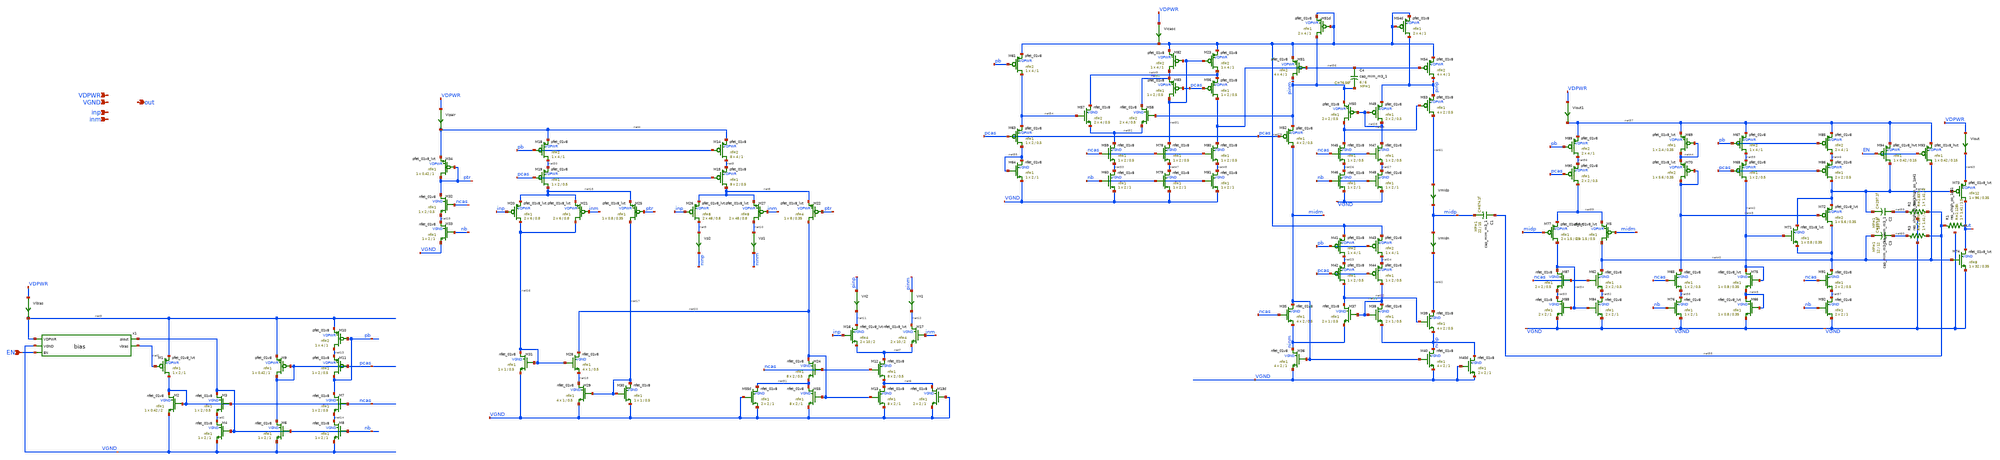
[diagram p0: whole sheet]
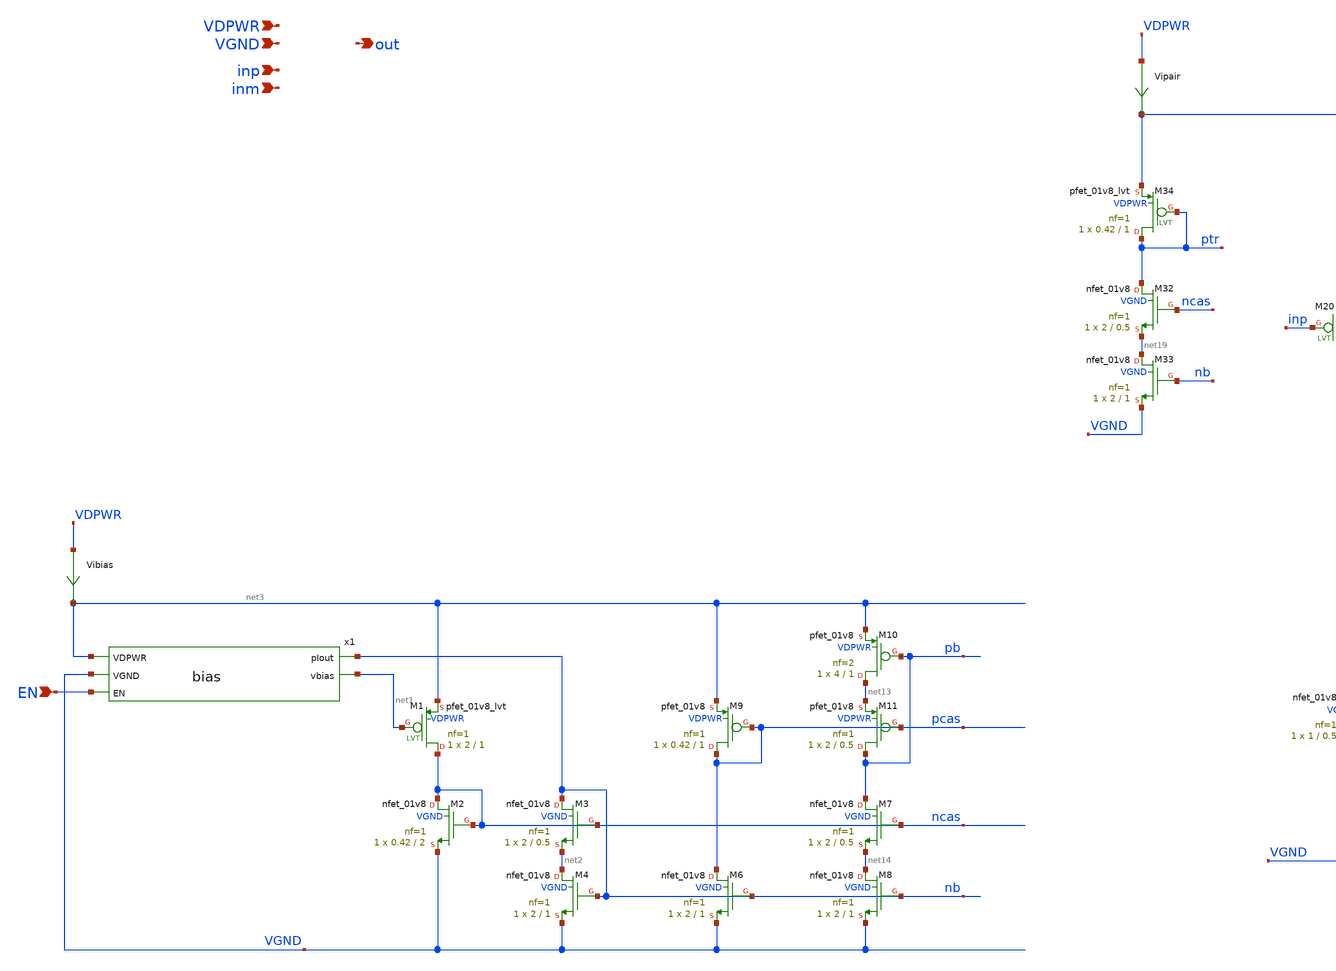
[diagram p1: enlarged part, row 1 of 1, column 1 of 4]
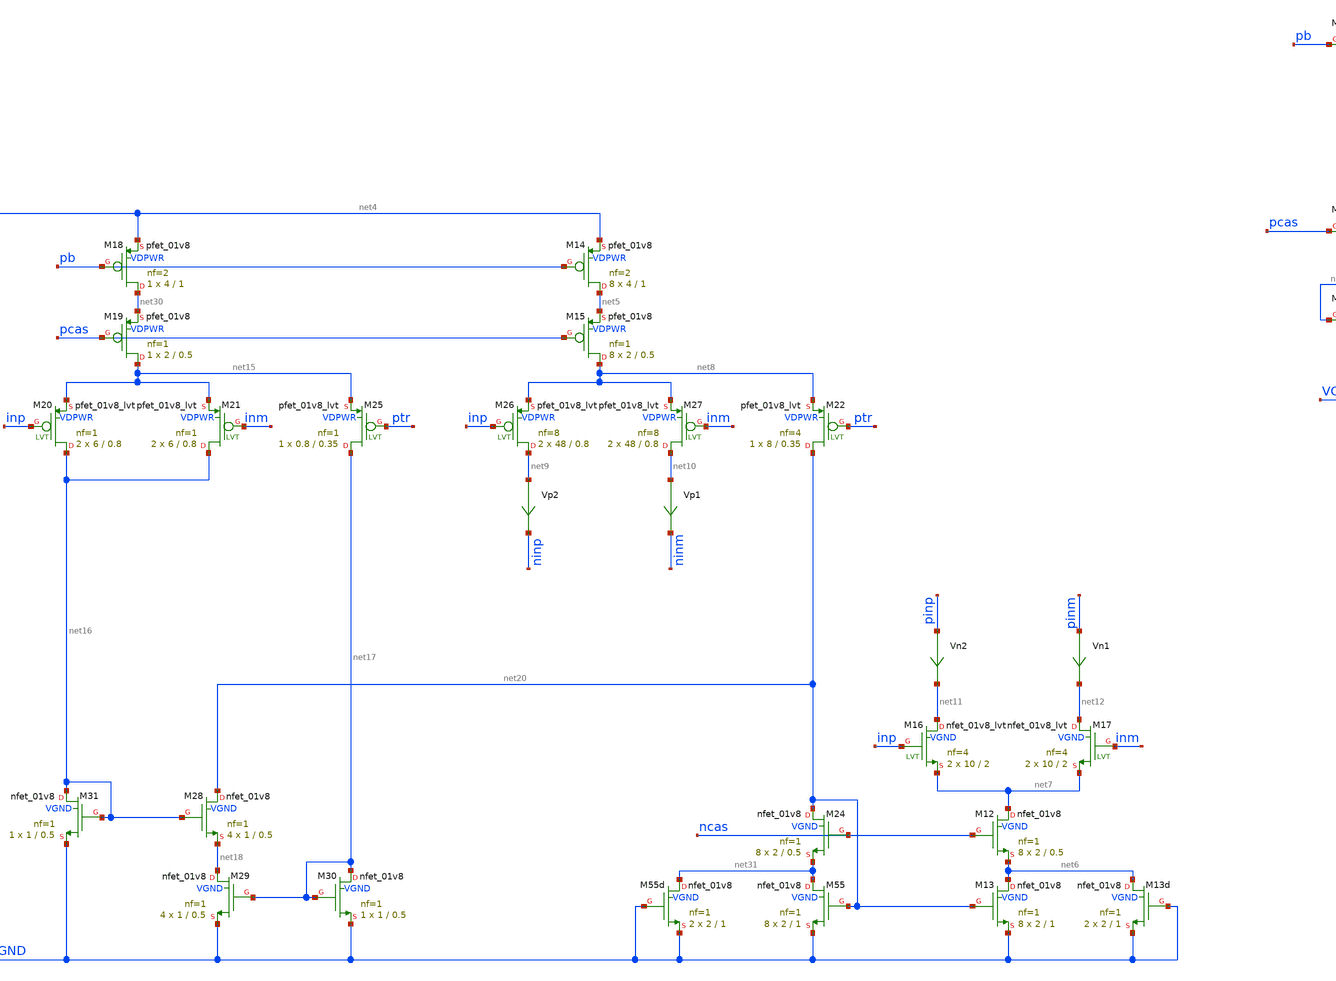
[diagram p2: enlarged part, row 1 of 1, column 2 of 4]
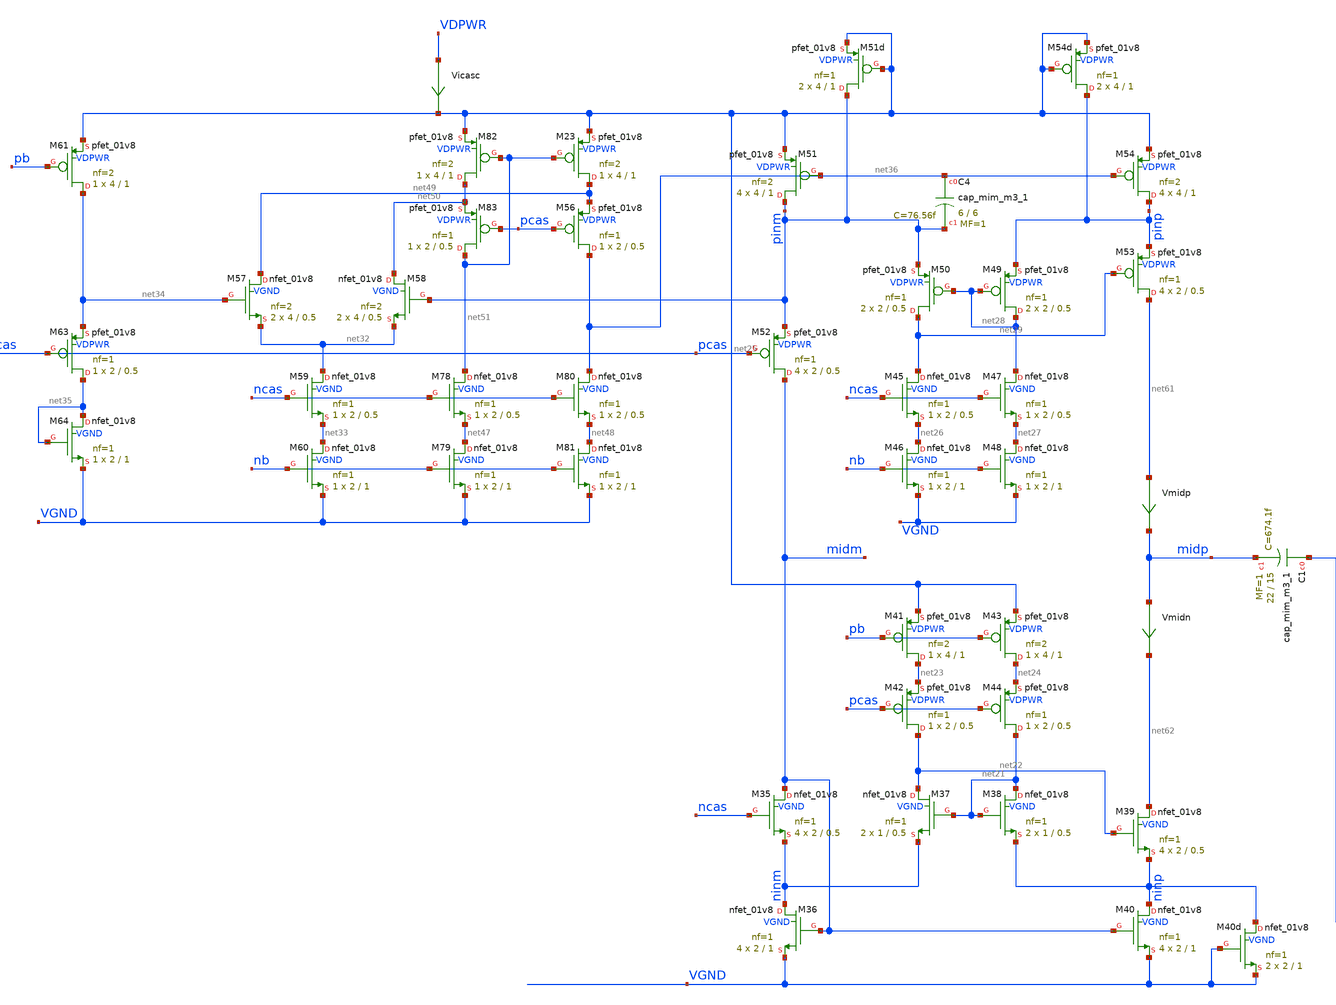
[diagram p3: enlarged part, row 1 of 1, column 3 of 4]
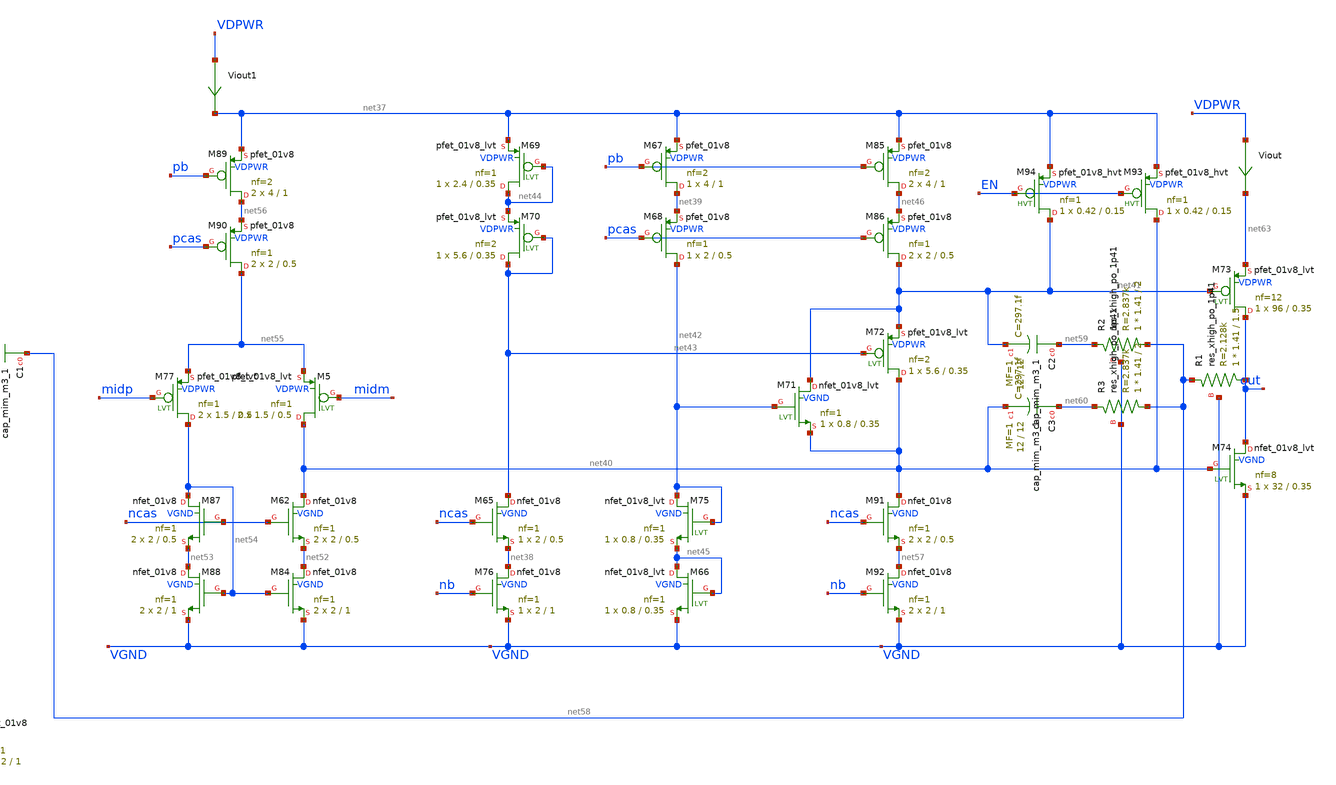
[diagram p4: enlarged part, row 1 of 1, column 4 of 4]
** sch_path: xschem/opamp.sch
**.subckt opamp VDPWR VGND inp inm out EN
*.ipin VDPWR
*.ipin VGND
*.ipin inp
*.ipin inm
*.opin out
*.ipin EN
x1 net3 nb VGND EN net1 bias
XM1 ncas net1 net3 VDPWR sky130_fd_pr__pfet_01v8_lvt L=1 W=2 nf=1 ad='int((1 + 1)/2) * 2 / 1 * 0.29'
+ as='int((1 + 2)/2) * 2 / 1 * 0.29' pd='2*int((1 + 1)/2) * (2 / 1 + 0.29)' ps='2*int((1 + 2)/2) * (2 / 1 + 0.29)'
+ nrd='0.29 / 2 ' nrs='0.29 / 2 ' sa=0 sb=0 sd=0 mult=1 m=1
XM2 ncas ncas VGND VGND sky130_fd_pr__nfet_01v8 L=2 W=0.42 nf=1 ad='int((1 + 1)/2) * 0.42 / 1 * 0.29'
+ as='int((1 + 2)/2) * 0.42 / 1 * 0.29' pd='2*int((1 + 1)/2) * (0.42 / 1 + 0.29)' ps='2*int((1 + 2)/2) * (0.42 / 1 + 0.29)'
+ nrd='0.29 / 0.42 ' nrs='0.29 / 0.42 ' sa=0 sb=0 sd=0 mult=1 m=1
XM3 nb ncas net2 VGND sky130_fd_pr__nfet_01v8 L=0.5 W=2 nf=1 ad='int((1 + 1)/2) * 2 / 1 * 0.29' as='int((1 + 2)/2) * 2 / 1 * 0.29'
+ pd='2*int((1 + 1)/2) * (2 / 1 + 0.29)' ps='2*int((1 + 2)/2) * (2 / 1 + 0.29)' nrd='0.29 / 2 ' nrs='0.29 / 2 '
+ sa=0 sb=0 sd=0 mult=1 m=1
XM4 net2 nb VGND VGND sky130_fd_pr__nfet_01v8 L=1 W=2 nf=1 ad='int((1 + 1)/2) * 2 / 1 * 0.29' as='int((1 + 2)/2) * 2 / 1 * 0.29'
+ pd='2*int((1 + 1)/2) * (2 / 1 + 0.29)' ps='2*int((1 + 2)/2) * (2 / 1 + 0.29)' nrd='0.29 / 2 ' nrs='0.29 / 2 '
+ sa=0 sb=0 sd=0 mult=1 m=1
XM6 pcas nb VGND VGND sky130_fd_pr__nfet_01v8 L=1 W=2 nf=1 ad='int((1 + 1)/2) * 2 / 1 * 0.29' as='int((1 + 2)/2) * 2 / 1 * 0.29'
+ pd='2*int((1 + 1)/2) * (2 / 1 + 0.29)' ps='2*int((1 + 2)/2) * (2 / 1 + 0.29)' nrd='0.29 / 2 ' nrs='0.29 / 2 '
+ sa=0 sb=0 sd=0 mult=1 m=1
XM7 pb ncas net14 VGND sky130_fd_pr__nfet_01v8 L=0.5 W=2 nf=1 ad='int((1 + 1)/2) * 2 / 1 * 0.29' as='int((1 + 2)/2) * 2 / 1 * 0.29'
+ pd='2*int((1 + 1)/2) * (2 / 1 + 0.29)' ps='2*int((1 + 2)/2) * (2 / 1 + 0.29)' nrd='0.29 / 2 ' nrs='0.29 / 2 '
+ sa=0 sb=0 sd=0 mult=1 m=1
XM8 net14 nb VGND VGND sky130_fd_pr__nfet_01v8 L=1 W=2 nf=1 ad='int((1 + 1)/2) * 2 / 1 * 0.29' as='int((1 + 2)/2) * 2 / 1 * 0.29'
+ pd='2*int((1 + 1)/2) * (2 / 1 + 0.29)' ps='2*int((1 + 2)/2) * (2 / 1 + 0.29)' nrd='0.29 / 2 ' nrs='0.29 / 2 '
+ sa=0 sb=0 sd=0 mult=1 m=1
XM9 pcas pcas net3 VDPWR sky130_fd_pr__pfet_01v8 L=1 W=0.42 nf=1 ad='int((1 + 1)/2) * 0.42 / 1 * 0.29'
+ as='int((1 + 2)/2) * 0.42 / 1 * 0.29' pd='2*int((1 + 1)/2) * (0.42 / 1 + 0.29)' ps='2*int((1 + 2)/2) * (0.42 / 1 + 0.29)'
+ nrd='0.29 / 0.42 ' nrs='0.29 / 0.42 ' sa=0 sb=0 sd=0 mult=1 m=1
XM10 net13 pb net3 VDPWR sky130_fd_pr__pfet_01v8 L=1 W=4 nf=2 ad='int((2 + 1)/2) * 4 / 2 * 0.29' as='int((2 + 2)/2) * 4 / 2 * 0.29'
+ pd='2*int((2 + 1)/2) * (4 / 2 + 0.29)' ps='2*int((2 + 2)/2) * (4 / 2 + 0.29)' nrd='0.29 / 4 ' nrs='0.29 / 4 '
+ sa=0 sb=0 sd=0 mult=1 m=1
XM11 pb pcas net13 VDPWR sky130_fd_pr__pfet_01v8 L=0.5 W=2 nf=1 ad='int((1 + 1)/2) * 2 / 1 * 0.29' as='int((1 + 2)/2) * 2 / 1 * 0.29'
+ pd='2*int((1 + 1)/2) * (2 / 1 + 0.29)' ps='2*int((1 + 2)/2) * (2 / 1 + 0.29)' nrd='0.29 / 2 ' nrs='0.29 / 2 '
+ sa=0 sb=0 sd=0 mult=1 m=1
XM12 net7 ncas net6 VGND sky130_fd_pr__nfet_01v8 L=0.5 W=2 nf=1 ad='int((1 + 1)/2) * 2 / 1 * 0.29' as='int((1 + 2)/2) * 2 / 1 * 0.29'
+ pd='2*int((1 + 1)/2) * (2 / 1 + 0.29)' ps='2*int((1 + 2)/2) * (2 / 1 + 0.29)' nrd='0.29 / 2 ' nrs='0.29 / 2 '
+ sa=0 sb=0 sd=0 mult=8 m=8
XM13 net6 net20 VGND VGND sky130_fd_pr__nfet_01v8 L=1 W=2 nf=1 ad='int((1 + 1)/2) * 2 / 1 * 0.29' as='int((1 + 2)/2) * 2 / 1 * 0.29'
+ pd='2*int((1 + 1)/2) * (2 / 1 + 0.29)' ps='2*int((1 + 2)/2) * (2 / 1 + 0.29)' nrd='0.29 / 2 ' nrs='0.29 / 2 '
+ sa=0 sb=0 sd=0 mult=8 m=8
XM14 net5 pb net4 VDPWR sky130_fd_pr__pfet_01v8 L=1 W=4 nf=2 ad='int((2 + 1)/2) * 4 / 2 * 0.29' as='int((2 + 2)/2) * 4 / 2 * 0.29'
+ pd='2*int((2 + 1)/2) * (4 / 2 + 0.29)' ps='2*int((2 + 2)/2) * (4 / 2 + 0.29)' nrd='0.29 / 4 ' nrs='0.29 / 4 '
+ sa=0 sb=0 sd=0 mult=8 m=8
XM15 net8 pcas net5 VDPWR sky130_fd_pr__pfet_01v8 L=0.5 W=2 nf=1 ad='int((1 + 1)/2) * 2 / 1 * 0.29' as='int((1 + 2)/2) * 2 / 1 * 0.29'
+ pd='2*int((1 + 1)/2) * (2 / 1 + 0.29)' ps='2*int((1 + 2)/2) * (2 / 1 + 0.29)' nrd='0.29 / 2 ' nrs='0.29 / 2 '
+ sa=0 sb=0 sd=0 mult=8 m=8
XM16 net11 inp net7 VGND sky130_fd_pr__nfet_01v8_lvt L=2 W=10 nf=4 ad='int((4 + 1)/2) * 10 / 4 * 0.29'
+ as='int((4 + 2)/2) * 10 / 4 * 0.29' pd='2*int((4 + 1)/2) * (10 / 4 + 0.29)' ps='2*int((4 + 2)/2) * (10 / 4 + 0.29)'
+ nrd='0.29 / 10 ' nrs='0.29 / 10 ' sa=0 sb=0 sd=0 mult=2 m=2
XM17 net12 inm net7 VGND sky130_fd_pr__nfet_01v8_lvt L=2 W=10 nf=4 ad='int((4 + 1)/2) * 10 / 4 * 0.29'
+ as='int((4 + 2)/2) * 10 / 4 * 0.29' pd='2*int((4 + 1)/2) * (10 / 4 + 0.29)' ps='2*int((4 + 2)/2) * (10 / 4 + 0.29)'
+ nrd='0.29 / 10 ' nrs='0.29 / 10 ' sa=0 sb=0 sd=0 mult=2 m=2
XM26 net9 inp net8 VDPWR sky130_fd_pr__pfet_01v8_lvt L=0.8 W=48 nf=8 ad='int((8 + 1)/2) * 48 / 8 * 0.29'
+ as='int((8 + 2)/2) * 48 / 8 * 0.29' pd='2*int((8 + 1)/2) * (48 / 8 + 0.29)' ps='2*int((8 + 2)/2) * (48 / 8 + 0.29)'
+ nrd='0.29 / 48 ' nrs='0.29 / 48 ' sa=0 sb=0 sd=0 mult=2 m=2
XM27 net10 inm net8 VDPWR sky130_fd_pr__pfet_01v8_lvt L=0.8 W=48 nf=8 ad='int((8 + 1)/2) * 48 / 8 * 0.29'
+ as='int((8 + 2)/2) * 48 / 8 * 0.29' pd='2*int((8 + 1)/2) * (48 / 8 + 0.29)' ps='2*int((8 + 2)/2) * (48 / 8 + 0.29)'
+ nrd='0.29 / 48 ' nrs='0.29 / 48 ' sa=0 sb=0 sd=0 mult=2 m=2
Vp1 net10 ninm 0
.save i(vp1)
Vp2 net9 ninp 0
.save i(vp2)
Vn1 pinm net12 0
.save i(vn1)
Vn2 pinp net11 0
.save i(vn2)
XM18 net30 pb net4 VDPWR sky130_fd_pr__pfet_01v8 L=1 W=4 nf=2 ad='int((2 + 1)/2) * 4 / 2 * 0.29' as='int((2 + 2)/2) * 4 / 2 * 0.29'
+ pd='2*int((2 + 1)/2) * (4 / 2 + 0.29)' ps='2*int((2 + 2)/2) * (4 / 2 + 0.29)' nrd='0.29 / 4 ' nrs='0.29 / 4 '
+ sa=0 sb=0 sd=0 mult=1 m=1
XM19 net15 pcas net30 VDPWR sky130_fd_pr__pfet_01v8 L=0.5 W=2 nf=1 ad='int((1 + 1)/2) * 2 / 1 * 0.29'
+ as='int((1 + 2)/2) * 2 / 1 * 0.29' pd='2*int((1 + 1)/2) * (2 / 1 + 0.29)' ps='2*int((1 + 2)/2) * (2 / 1 + 0.29)'
+ nrd='0.29 / 2 ' nrs='0.29 / 2 ' sa=0 sb=0 sd=0 mult=1 m=1
XM20 net16 inp net15 VDPWR sky130_fd_pr__pfet_01v8_lvt L=0.8 W=6 nf=1 ad='int((1 + 1)/2) * 6 / 1 * 0.29'
+ as='int((1 + 2)/2) * 6 / 1 * 0.29' pd='2*int((1 + 1)/2) * (6 / 1 + 0.29)' ps='2*int((1 + 2)/2) * (6 / 1 + 0.29)'
+ nrd='0.29 / 6 ' nrs='0.29 / 6 ' sa=0 sb=0 sd=0 mult=2 m=2
XM21 net16 inm net15 VDPWR sky130_fd_pr__pfet_01v8_lvt L=0.8 W=6 nf=1 ad='int((1 + 1)/2) * 6 / 1 * 0.29'
+ as='int((1 + 2)/2) * 6 / 1 * 0.29' pd='2*int((1 + 1)/2) * (6 / 1 + 0.29)' ps='2*int((1 + 2)/2) * (6 / 1 + 0.29)'
+ nrd='0.29 / 6 ' nrs='0.29 / 6 ' sa=0 sb=0 sd=0 mult=2 m=2
XM25 net17 ptr net15 VDPWR sky130_fd_pr__pfet_01v8_lvt L=0.35 W=0.8 nf=1 ad='int((1 + 1)/2) * 0.8 / 1 * 0.29'
+ as='int((1 + 2)/2) * 0.8 / 1 * 0.29' pd='2*int((1 + 1)/2) * (0.8 / 1 + 0.29)' ps='2*int((1 + 2)/2) * (0.8 / 1 + 0.29)'
+ nrd='0.29 / 0.8 ' nrs='0.29 / 0.8 ' sa=0 sb=0 sd=0 mult=1 m=1
XM28 net20 net16 net18 VGND sky130_fd_pr__nfet_01v8 L=0.5 W=1 nf=1 ad='int((1 + 1)/2) * 1 / 1 * 0.29'
+ as='int((1 + 2)/2) * 1 / 1 * 0.29' pd='2*int((1 + 1)/2) * (1 / 1 + 0.29)' ps='2*int((1 + 2)/2) * (1 / 1 + 0.29)'
+ nrd='0.29 / 1 ' nrs='0.29 / 1 ' sa=0 sb=0 sd=0 mult=4 m=4
XM29 net18 net17 VGND VGND sky130_fd_pr__nfet_01v8 L=0.5 W=1 nf=1 ad='int((1 + 1)/2) * 1 / 1 * 0.29'
+ as='int((1 + 2)/2) * 1 / 1 * 0.29' pd='2*int((1 + 1)/2) * (1 / 1 + 0.29)' ps='2*int((1 + 2)/2) * (1 / 1 + 0.29)'
+ nrd='0.29 / 1 ' nrs='0.29 / 1 ' sa=0 sb=0 sd=0 mult=4 m=4
XM30 net17 net17 VGND VGND sky130_fd_pr__nfet_01v8 L=0.5 W=1 nf=1 ad='int((1 + 1)/2) * 1 / 1 * 0.29'
+ as='int((1 + 2)/2) * 1 / 1 * 0.29' pd='2*int((1 + 1)/2) * (1 / 1 + 0.29)' ps='2*int((1 + 2)/2) * (1 / 1 + 0.29)'
+ nrd='0.29 / 1 ' nrs='0.29 / 1 ' sa=0 sb=0 sd=0 mult=1 m=1
XM31 net16 net16 VGND VGND sky130_fd_pr__nfet_01v8 L=0.5 W=1 nf=1 ad='int((1 + 1)/2) * 1 / 1 * 0.29'
+ as='int((1 + 2)/2) * 1 / 1 * 0.29' pd='2*int((1 + 1)/2) * (1 / 1 + 0.29)' ps='2*int((1 + 2)/2) * (1 / 1 + 0.29)'
+ nrd='0.29 / 1 ' nrs='0.29 / 1 ' sa=0 sb=0 sd=0 mult=1 m=1
XM32 ptr ncas net19 VGND sky130_fd_pr__nfet_01v8 L=0.5 W=2 nf=1 ad='int((1 + 1)/2) * 2 / 1 * 0.29' as='int((1 + 2)/2) * 2 / 1 * 0.29'
+ pd='2*int((1 + 1)/2) * (2 / 1 + 0.29)' ps='2*int((1 + 2)/2) * (2 / 1 + 0.29)' nrd='0.29 / 2 ' nrs='0.29 / 2 '
+ sa=0 sb=0 sd=0 mult=1 m=1
XM33 net19 nb VGND VGND sky130_fd_pr__nfet_01v8 L=1 W=2 nf=1 ad='int((1 + 1)/2) * 2 / 1 * 0.29' as='int((1 + 2)/2) * 2 / 1 * 0.29'
+ pd='2*int((1 + 1)/2) * (2 / 1 + 0.29)' ps='2*int((1 + 2)/2) * (2 / 1 + 0.29)' nrd='0.29 / 2 ' nrs='0.29 / 2 '
+ sa=0 sb=0 sd=0 mult=1 m=1
XM34 ptr ptr net4 VDPWR sky130_fd_pr__pfet_01v8_lvt L=1 W=0.42 nf=1 ad='int((1 + 1)/2) * 0.42 / 1 * 0.29'
+ as='int((1 + 2)/2) * 0.42 / 1 * 0.29' pd='2*int((1 + 1)/2) * (0.42 / 1 + 0.29)' ps='2*int((1 + 2)/2) * (0.42 / 1 + 0.29)'
+ nrd='0.29 / 0.42 ' nrs='0.29 / 0.42 ' sa=0 sb=0 sd=0 mult=1 m=1
XM35 midm ncas ninm VGND sky130_fd_pr__nfet_01v8 L=0.5 W=2 nf=1 ad='int((1 + 1)/2) * 2 / 1 * 0.29' as='int((1 + 2)/2) * 2 / 1 * 0.29'
+ pd='2*int((1 + 1)/2) * (2 / 1 + 0.29)' ps='2*int((1 + 2)/2) * (2 / 1 + 0.29)' nrd='0.29 / 2 ' nrs='0.29 / 2 '
+ sa=0 sb=0 sd=0 mult=4 m=4
XM36 ninm midm VGND VGND sky130_fd_pr__nfet_01v8 L=1 W=2 nf=1 ad='int((1 + 1)/2) * 2 / 1 * 0.29' as='int((1 + 2)/2) * 2 / 1 * 0.29'
+ pd='2*int((1 + 1)/2) * (2 / 1 + 0.29)' ps='2*int((1 + 2)/2) * (2 / 1 + 0.29)' nrd='0.29 / 2 ' nrs='0.29 / 2 '
+ sa=0 sb=0 sd=0 mult=4 m=4
XM37 net22 net21 ninm VGND sky130_fd_pr__nfet_01v8 L=0.5 W=1 nf=1 ad='int((1 + 1)/2) * 1 / 1 * 0.29'
+ as='int((1 + 2)/2) * 1 / 1 * 0.29' pd='2*int((1 + 1)/2) * (1 / 1 + 0.29)' ps='2*int((1 + 2)/2) * (1 / 1 + 0.29)'
+ nrd='0.29 / 1 ' nrs='0.29 / 1 ' sa=0 sb=0 sd=0 mult=2 m=2
XM39 net62 net22 ninp VGND sky130_fd_pr__nfet_01v8 L=0.5 W=2 nf=1 ad='int((1 + 1)/2) * 2 / 1 * 0.29'
+ as='int((1 + 2)/2) * 2 / 1 * 0.29' pd='2*int((1 + 1)/2) * (2 / 1 + 0.29)' ps='2*int((1 + 2)/2) * (2 / 1 + 0.29)'
+ nrd='0.29 / 2 ' nrs='0.29 / 2 ' sa=0 sb=0 sd=0 mult=4 m=4
XM40 ninp midm VGND VGND sky130_fd_pr__nfet_01v8 L=1 W=2 nf=1 ad='int((1 + 1)/2) * 2 / 1 * 0.29' as='int((1 + 2)/2) * 2 / 1 * 0.29'
+ pd='2*int((1 + 1)/2) * (2 / 1 + 0.29)' ps='2*int((1 + 2)/2) * (2 / 1 + 0.29)' nrd='0.29 / 2 ' nrs='0.29 / 2 '
+ sa=0 sb=0 sd=0 mult=4 m=4
XM41 net23 pb net25 VDPWR sky130_fd_pr__pfet_01v8 L=1 W=4 nf=2 ad='int((2 + 1)/2) * 4 / 2 * 0.29' as='int((2 + 2)/2) * 4 / 2 * 0.29'
+ pd='2*int((2 + 1)/2) * (4 / 2 + 0.29)' ps='2*int((2 + 2)/2) * (4 / 2 + 0.29)' nrd='0.29 / 4 ' nrs='0.29 / 4 '
+ sa=0 sb=0 sd=0 mult=1 m=1
XM42 net22 pcas net23 VDPWR sky130_fd_pr__pfet_01v8 L=0.5 W=2 nf=1 ad='int((1 + 1)/2) * 2 / 1 * 0.29'
+ as='int((1 + 2)/2) * 2 / 1 * 0.29' pd='2*int((1 + 1)/2) * (2 / 1 + 0.29)' ps='2*int((1 + 2)/2) * (2 / 1 + 0.29)'
+ nrd='0.29 / 2 ' nrs='0.29 / 2 ' sa=0 sb=0 sd=0 mult=1 m=1
XM43 net24 pb net25 VDPWR sky130_fd_pr__pfet_01v8 L=1 W=4 nf=2 ad='int((2 + 1)/2) * 4 / 2 * 0.29' as='int((2 + 2)/2) * 4 / 2 * 0.29'
+ pd='2*int((2 + 1)/2) * (4 / 2 + 0.29)' ps='2*int((2 + 2)/2) * (4 / 2 + 0.29)' nrd='0.29 / 4 ' nrs='0.29 / 4 '
+ sa=0 sb=0 sd=0 mult=1 m=1
XM44 net21 pcas net24 VDPWR sky130_fd_pr__pfet_01v8 L=0.5 W=2 nf=1 ad='int((1 + 1)/2) * 2 / 1 * 0.29'
+ as='int((1 + 2)/2) * 2 / 1 * 0.29' pd='2*int((1 + 1)/2) * (2 / 1 + 0.29)' ps='2*int((1 + 2)/2) * (2 / 1 + 0.29)'
+ nrd='0.29 / 2 ' nrs='0.29 / 2 ' sa=0 sb=0 sd=0 mult=1 m=1
XM45 net29 ncas net26 VGND sky130_fd_pr__nfet_01v8 L=0.5 W=2 nf=1 ad='int((1 + 1)/2) * 2 / 1 * 0.29'
+ as='int((1 + 2)/2) * 2 / 1 * 0.29' pd='2*int((1 + 1)/2) * (2 / 1 + 0.29)' ps='2*int((1 + 2)/2) * (2 / 1 + 0.29)'
+ nrd='0.29 / 2 ' nrs='0.29 / 2 ' sa=0 sb=0 sd=0 mult=1 m=1
XM46 net26 nb VGND VGND sky130_fd_pr__nfet_01v8 L=1 W=2 nf=1 ad='int((1 + 1)/2) * 2 / 1 * 0.29' as='int((1 + 2)/2) * 2 / 1 * 0.29'
+ pd='2*int((1 + 1)/2) * (2 / 1 + 0.29)' ps='2*int((1 + 2)/2) * (2 / 1 + 0.29)' nrd='0.29 / 2 ' nrs='0.29 / 2 '
+ sa=0 sb=0 sd=0 mult=1 m=1
XM47 net28 ncas net27 VGND sky130_fd_pr__nfet_01v8 L=0.5 W=2 nf=1 ad='int((1 + 1)/2) * 2 / 1 * 0.29'
+ as='int((1 + 2)/2) * 2 / 1 * 0.29' pd='2*int((1 + 1)/2) * (2 / 1 + 0.29)' ps='2*int((1 + 2)/2) * (2 / 1 + 0.29)'
+ nrd='0.29 / 2 ' nrs='0.29 / 2 ' sa=0 sb=0 sd=0 mult=1 m=1
XM48 net27 nb VGND VGND sky130_fd_pr__nfet_01v8 L=1 W=2 nf=1 ad='int((1 + 1)/2) * 2 / 1 * 0.29' as='int((1 + 2)/2) * 2 / 1 * 0.29'
+ pd='2*int((1 + 1)/2) * (2 / 1 + 0.29)' ps='2*int((1 + 2)/2) * (2 / 1 + 0.29)' nrd='0.29 / 2 ' nrs='0.29 / 2 '
+ sa=0 sb=0 sd=0 mult=1 m=1
XM50 net29 net28 pinm VDPWR sky130_fd_pr__pfet_01v8 L=0.5 W=2 nf=1 ad='int((1 + 1)/2) * 2 / 1 * 0.29'
+ as='int((1 + 2)/2) * 2 / 1 * 0.29' pd='2*int((1 + 1)/2) * (2 / 1 + 0.29)' ps='2*int((1 + 2)/2) * (2 / 1 + 0.29)'
+ nrd='0.29 / 2 ' nrs='0.29 / 2 ' sa=0 sb=0 sd=0 mult=2 m=2
XM51 pinm net36 net25 VDPWR sky130_fd_pr__pfet_01v8 L=1 W=4 nf=2 ad='int((2 + 1)/2) * 4 / 2 * 0.29' as='int((2 + 2)/2) * 4 / 2 * 0.29'
+ pd='2*int((2 + 1)/2) * (4 / 2 + 0.29)' ps='2*int((2 + 2)/2) * (4 / 2 + 0.29)' nrd='0.29 / 4 ' nrs='0.29 / 4 '
+ sa=0 sb=0 sd=0 mult=4 m=4
XM52 midm pcas pinm VDPWR sky130_fd_pr__pfet_01v8 L=0.5 W=2 nf=1 ad='int((1 + 1)/2) * 2 / 1 * 0.29' as='int((1 + 2)/2) * 2 / 1 * 0.29'
+ pd='2*int((1 + 1)/2) * (2 / 1 + 0.29)' ps='2*int((1 + 2)/2) * (2 / 1 + 0.29)' nrd='0.29 / 2 ' nrs='0.29 / 2 '
+ sa=0 sb=0 sd=0 mult=4 m=4
XM53 net61 net29 pinp VDPWR sky130_fd_pr__pfet_01v8 L=0.5 W=2 nf=1 ad='int((1 + 1)/2) * 2 / 1 * 0.29'
+ as='int((1 + 2)/2) * 2 / 1 * 0.29' pd='2*int((1 + 1)/2) * (2 / 1 + 0.29)' ps='2*int((1 + 2)/2) * (2 / 1 + 0.29)'
+ nrd='0.29 / 2 ' nrs='0.29 / 2 ' sa=0 sb=0 sd=0 mult=4 m=4
XM54 pinp net36 net25 VDPWR sky130_fd_pr__pfet_01v8 L=1 W=4 nf=2 ad='int((2 + 1)/2) * 4 / 2 * 0.29' as='int((2 + 2)/2) * 4 / 2 * 0.29'
+ pd='2*int((2 + 1)/2) * (4 / 2 + 0.29)' ps='2*int((2 + 2)/2) * (4 / 2 + 0.29)' nrd='0.29 / 4 ' nrs='0.29 / 4 '
+ sa=0 sb=0 sd=0 mult=4 m=4
Vibias VDPWR net3 0
.save i(vibias)
Vipair VDPWR net4 0
.save i(vipair)
Vicasc VDPWR net25 0
.save i(vicasc)
XM49 net28 net28 pinp VDPWR sky130_fd_pr__pfet_01v8 L=0.5 W=2 nf=1 ad='int((1 + 1)/2) * 2 / 1 * 0.29'
+ as='int((1 + 2)/2) * 2 / 1 * 0.29' pd='2*int((1 + 1)/2) * (2 / 1 + 0.29)' ps='2*int((1 + 2)/2) * (2 / 1 + 0.29)'
+ nrd='0.29 / 2 ' nrs='0.29 / 2 ' sa=0 sb=0 sd=0 mult=2 m=2
XM38 net21 net21 ninp VGND sky130_fd_pr__nfet_01v8 L=0.5 W=1 nf=1 ad='int((1 + 1)/2) * 1 / 1 * 0.29'
+ as='int((1 + 2)/2) * 1 / 1 * 0.29' pd='2*int((1 + 1)/2) * (1 / 1 + 0.29)' ps='2*int((1 + 2)/2) * (1 / 1 + 0.29)'
+ nrd='0.29 / 1 ' nrs='0.29 / 1 ' sa=0 sb=0 sd=0 mult=2 m=2
XM24 net20 ncas net31 VGND sky130_fd_pr__nfet_01v8 L=0.5 W=2 nf=1 ad='int((1 + 1)/2) * 2 / 1 * 0.29'
+ as='int((1 + 2)/2) * 2 / 1 * 0.29' pd='2*int((1 + 1)/2) * (2 / 1 + 0.29)' ps='2*int((1 + 2)/2) * (2 / 1 + 0.29)'
+ nrd='0.29 / 2 ' nrs='0.29 / 2 ' sa=0 sb=0 sd=0 mult=8 m=8
XM55 net31 net20 VGND VGND sky130_fd_pr__nfet_01v8 L=1 W=2 nf=1 ad='int((1 + 1)/2) * 2 / 1 * 0.29' as='int((1 + 2)/2) * 2 / 1 * 0.29'
+ pd='2*int((1 + 1)/2) * (2 / 1 + 0.29)' ps='2*int((1 + 2)/2) * (2 / 1 + 0.29)' nrd='0.29 / 2 ' nrs='0.29 / 2 '
+ sa=0 sb=0 sd=0 mult=8 m=8
XM22 net20 ptr net8 VDPWR sky130_fd_pr__pfet_01v8_lvt L=0.35 W=8 nf=4 ad='int((4 + 1)/2) * 8 / 4 * 0.29'
+ as='int((4 + 2)/2) * 8 / 4 * 0.29' pd='2*int((4 + 1)/2) * (8 / 4 + 0.29)' ps='2*int((4 + 2)/2) * (8 / 4 + 0.29)'
+ nrd='0.29 / 8 ' nrs='0.29 / 8 ' sa=0 sb=0 sd=0 mult=1 m=1
XM57 net49 net34 net32 VGND sky130_fd_pr__nfet_01v8 L=0.5 W=4 nf=2 ad='int((2 + 1)/2) * 4 / 2 * 0.29'
+ as='int((2 + 2)/2) * 4 / 2 * 0.29' pd='2*int((2 + 1)/2) * (4 / 2 + 0.29)' ps='2*int((2 + 2)/2) * (4 / 2 + 0.29)'
+ nrd='0.29 / 4 ' nrs='0.29 / 4 ' sa=0 sb=0 sd=0 mult=2 m=2
XM58 net50 pinm net32 VGND sky130_fd_pr__nfet_01v8 L=0.5 W=4 nf=2 ad='int((2 + 1)/2) * 4 / 2 * 0.29'
+ as='int((2 + 2)/2) * 4 / 2 * 0.29' pd='2*int((2 + 1)/2) * (4 / 2 + 0.29)' ps='2*int((2 + 2)/2) * (4 / 2 + 0.29)'
+ nrd='0.29 / 4 ' nrs='0.29 / 4 ' sa=0 sb=0 sd=0 mult=2 m=2
XM59 net32 ncas net33 VGND sky130_fd_pr__nfet_01v8 L=0.5 W=2 nf=1 ad='int((1 + 1)/2) * 2 / 1 * 0.29'
+ as='int((1 + 2)/2) * 2 / 1 * 0.29' pd='2*int((1 + 1)/2) * (2 / 1 + 0.29)' ps='2*int((1 + 2)/2) * (2 / 1 + 0.29)'
+ nrd='0.29 / 2 ' nrs='0.29 / 2 ' sa=0 sb=0 sd=0 mult=1 m=1
XM60 net33 nb VGND VGND sky130_fd_pr__nfet_01v8 L=1 W=2 nf=1 ad='int((1 + 1)/2) * 2 / 1 * 0.29' as='int((1 + 2)/2) * 2 / 1 * 0.29'
+ pd='2*int((1 + 1)/2) * (2 / 1 + 0.29)' ps='2*int((1 + 2)/2) * (2 / 1 + 0.29)' nrd='0.29 / 2 ' nrs='0.29 / 2 '
+ sa=0 sb=0 sd=0 mult=1 m=1
XM61 net34 pb net25 VDPWR sky130_fd_pr__pfet_01v8 L=1 W=4 nf=2 ad='int((2 + 1)/2) * 4 / 2 * 0.29' as='int((2 + 2)/2) * 4 / 2 * 0.29'
+ pd='2*int((2 + 1)/2) * (4 / 2 + 0.29)' ps='2*int((2 + 2)/2) * (4 / 2 + 0.29)' nrd='0.29 / 4 ' nrs='0.29 / 4 '
+ sa=0 sb=0 sd=0 mult=1 m=1
XM63 net35 pcas net34 VDPWR sky130_fd_pr__pfet_01v8 L=0.5 W=2 nf=1 ad='int((1 + 1)/2) * 2 / 1 * 0.29'
+ as='int((1 + 2)/2) * 2 / 1 * 0.29' pd='2*int((1 + 1)/2) * (2 / 1 + 0.29)' ps='2*int((1 + 2)/2) * (2 / 1 + 0.29)'
+ nrd='0.29 / 2 ' nrs='0.29 / 2 ' sa=0 sb=0 sd=0 mult=1 m=1
XM64 net35 net35 VGND VGND sky130_fd_pr__nfet_01v8 L=1 W=2 nf=1 ad='int((1 + 1)/2) * 2 / 1 * 0.29' as='int((1 + 2)/2) * 2 / 1 * 0.29'
+ pd='2*int((1 + 1)/2) * (2 / 1 + 0.29)' ps='2*int((1 + 2)/2) * (2 / 1 + 0.29)' nrd='0.29 / 2 ' nrs='0.29 / 2 '
+ sa=0 sb=0 sd=0 mult=1 m=1
XM65 net43 ncas net38 VGND sky130_fd_pr__nfet_01v8 L=0.5 W=2 nf=1 ad='int((1 + 1)/2) * 2 / 1 * 0.29'
+ as='int((1 + 2)/2) * 2 / 1 * 0.29' pd='2*int((1 + 1)/2) * (2 / 1 + 0.29)' ps='2*int((1 + 2)/2) * (2 / 1 + 0.29)'
+ nrd='0.29 / 2 ' nrs='0.29 / 2 ' sa=0 sb=0 sd=0 mult=1 m=1
XM66 net45 net45 VGND VGND sky130_fd_pr__nfet_01v8_lvt L=0.35 W=0.8 nf=1 ad='int((1 + 1)/2) * 0.8 / 1 * 0.29'
+ as='int((1 + 2)/2) * 0.8 / 1 * 0.29' pd='2*int((1 + 1)/2) * (0.8 / 1 + 0.29)' ps='2*int((1 + 2)/2) * (0.8 / 1 + 0.29)'
+ nrd='0.29 / 0.8 ' nrs='0.29 / 0.8 ' sa=0 sb=0 sd=0 mult=1 m=1
XM67 net39 pb net37 VDPWR sky130_fd_pr__pfet_01v8 L=1 W=4 nf=2 ad='int((2 + 1)/2) * 4 / 2 * 0.29' as='int((2 + 2)/2) * 4 / 2 * 0.29'
+ pd='2*int((2 + 1)/2) * (4 / 2 + 0.29)' ps='2*int((2 + 2)/2) * (4 / 2 + 0.29)' nrd='0.29 / 4 ' nrs='0.29 / 4 '
+ sa=0 sb=0 sd=0 mult=1 m=1
XM68 net42 pcas net39 VDPWR sky130_fd_pr__pfet_01v8 L=0.5 W=2 nf=1 ad='int((1 + 1)/2) * 2 / 1 * 0.29'
+ as='int((1 + 2)/2) * 2 / 1 * 0.29' pd='2*int((1 + 1)/2) * (2 / 1 + 0.29)' ps='2*int((1 + 2)/2) * (2 / 1 + 0.29)'
+ nrd='0.29 / 2 ' nrs='0.29 / 2 ' sa=0 sb=0 sd=0 mult=1 m=1
XM69 net44 net44 net37 VDPWR sky130_fd_pr__pfet_01v8_lvt L=0.35 W=2.4 nf=1 ad='int((1 + 1)/2) * 2.4 / 1 * 0.29'
+ as='int((1 + 2)/2) * 2.4 / 1 * 0.29' pd='2*int((1 + 1)/2) * (2.4 / 1 + 0.29)' ps='2*int((1 + 2)/2) * (2.4 / 1 + 0.29)'
+ nrd='0.29 / 2.4 ' nrs='0.29 / 2.4 ' sa=0 sb=0 sd=0 mult=1 m=1
XM70 net43 net43 net44 VDPWR sky130_fd_pr__pfet_01v8_lvt L=0.35 W=5.6 nf=2 ad='int((2 + 1)/2) * 5.6 / 2 * 0.29'
+ as='int((2 + 2)/2) * 5.6 / 2 * 0.29' pd='2*int((2 + 1)/2) * (5.6 / 2 + 0.29)' ps='2*int((2 + 2)/2) * (5.6 / 2 + 0.29)'
+ nrd='0.29 / 5.6 ' nrs='0.29 / 5.6 ' sa=0 sb=0 sd=0 mult=1 m=1
XM71 net41 net42 net40 VGND sky130_fd_pr__nfet_01v8_lvt L=0.35 W=0.8 nf=1 ad='int((1 + 1)/2) * 0.8 / 1 * 0.29'
+ as='int((1 + 2)/2) * 0.8 / 1 * 0.29' pd='2*int((1 + 1)/2) * (0.8 / 1 + 0.29)' ps='2*int((1 + 2)/2) * (0.8 / 1 + 0.29)'
+ nrd='0.29 / 0.8 ' nrs='0.29 / 0.8 ' sa=0 sb=0 sd=0 mult=1 m=1
XM72 net40 net43 net41 VDPWR sky130_fd_pr__pfet_01v8_lvt L=0.35 W=5.6 nf=2 ad='int((2 + 1)/2) * 5.6 / 2 * 0.29'
+ as='int((2 + 2)/2) * 5.6 / 2 * 0.29' pd='2*int((2 + 1)/2) * (5.6 / 2 + 0.29)' ps='2*int((2 + 2)/2) * (5.6 / 2 + 0.29)'
+ nrd='0.29 / 5.6 ' nrs='0.29 / 5.6 ' sa=0 sb=0 sd=0 mult=1 m=1
Viout VDPWR net63 0
.save i(viout)
XM73 out net41 net63 VDPWR sky130_fd_pr__pfet_01v8_lvt L=0.35 W=96 nf=12 ad='int((12 + 1)/2) * 96 / 12 * 0.29'
+ as='int((12 + 2)/2) * 96 / 12 * 0.29' pd='2*int((12 + 1)/2) * (96 / 12 + 0.29)' ps='2*int((12 + 2)/2) * (96 / 12 + 0.29)'
+ nrd='0.29 / 96 ' nrs='0.29 / 96 ' sa=0 sb=0 sd=0 mult=1 m=1
XM74 out net40 VGND VGND sky130_fd_pr__nfet_01v8_lvt L=0.35 W=32 nf=8 ad='int((8 + 1)/2) * 32 / 8 * 0.29'
+ as='int((8 + 2)/2) * 32 / 8 * 0.29' pd='2*int((8 + 1)/2) * (32 / 8 + 0.29)' ps='2*int((8 + 2)/2) * (32 / 8 + 0.29)'
+ nrd='0.29 / 32 ' nrs='0.29 / 32 ' sa=0 sb=0 sd=0 mult=1 m=1
XM75 net42 net42 net45 VGND sky130_fd_pr__nfet_01v8_lvt L=0.35 W=0.8 nf=1 ad='int((1 + 1)/2) * 0.8 / 1 * 0.29'
+ as='int((1 + 2)/2) * 0.8 / 1 * 0.29' pd='2*int((1 + 1)/2) * (0.8 / 1 + 0.29)' ps='2*int((1 + 2)/2) * (0.8 / 1 + 0.29)'
+ nrd='0.29 / 0.8 ' nrs='0.29 / 0.8 ' sa=0 sb=0 sd=0 mult=1 m=1
XM76 net38 nb VGND VGND sky130_fd_pr__nfet_01v8 L=1 W=2 nf=1 ad='int((1 + 1)/2) * 2 / 1 * 0.29' as='int((1 + 2)/2) * 2 / 1 * 0.29'
+ pd='2*int((1 + 1)/2) * (2 / 1 + 0.29)' ps='2*int((1 + 2)/2) * (2 / 1 + 0.29)' nrd='0.29 / 2 ' nrs='0.29 / 2 '
+ sa=0 sb=0 sd=0 mult=1 m=1
XM85 net46 pb net37 VDPWR sky130_fd_pr__pfet_01v8 L=1 W=4 nf=2 ad='int((2 + 1)/2) * 4 / 2 * 0.29' as='int((2 + 2)/2) * 4 / 2 * 0.29'
+ pd='2*int((2 + 1)/2) * (4 / 2 + 0.29)' ps='2*int((2 + 2)/2) * (4 / 2 + 0.29)' nrd='0.29 / 4 ' nrs='0.29 / 4 '
+ sa=0 sb=0 sd=0 mult=2 m=2
XM86 net41 pcas net46 VDPWR sky130_fd_pr__pfet_01v8 L=0.5 W=2 nf=1 ad='int((1 + 1)/2) * 2 / 1 * 0.29'
+ as='int((1 + 2)/2) * 2 / 1 * 0.29' pd='2*int((1 + 1)/2) * (2 / 1 + 0.29)' ps='2*int((1 + 2)/2) * (2 / 1 + 0.29)'
+ nrd='0.29 / 2 ' nrs='0.29 / 2 ' sa=0 sb=0 sd=0 mult=2 m=2
XM77 net54 midp net55 VDPWR sky130_fd_pr__pfet_01v8_lvt L=0.5 W=1.5 nf=1 ad='int((1 + 1)/2) * 1.5 / 1 * 0.29'
+ as='int((1 + 2)/2) * 1.5 / 1 * 0.29' pd='2*int((1 + 1)/2) * (1.5 / 1 + 0.29)' ps='2*int((1 + 2)/2) * (1.5 / 1 + 0.29)'
+ nrd='0.29 / 1.5 ' nrs='0.29 / 1.5 ' sa=0 sb=0 sd=0 mult=2 m=2
Viout1 VDPWR net37 0
.save i(viout1)
XM78 net51 ncas net47 VGND sky130_fd_pr__nfet_01v8 L=0.5 W=2 nf=1 ad='int((1 + 1)/2) * 2 / 1 * 0.29'
+ as='int((1 + 2)/2) * 2 / 1 * 0.29' pd='2*int((1 + 1)/2) * (2 / 1 + 0.29)' ps='2*int((1 + 2)/2) * (2 / 1 + 0.29)'
+ nrd='0.29 / 2 ' nrs='0.29 / 2 ' sa=0 sb=0 sd=0 mult=1 m=1
XM79 net47 nb VGND VGND sky130_fd_pr__nfet_01v8 L=1 W=2 nf=1 ad='int((1 + 1)/2) * 2 / 1 * 0.29' as='int((1 + 2)/2) * 2 / 1 * 0.29'
+ pd='2*int((1 + 1)/2) * (2 / 1 + 0.29)' ps='2*int((1 + 2)/2) * (2 / 1 + 0.29)' nrd='0.29 / 2 ' nrs='0.29 / 2 '
+ sa=0 sb=0 sd=0 mult=1 m=1
XM80 net36 ncas net48 VGND sky130_fd_pr__nfet_01v8 L=0.5 W=2 nf=1 ad='int((1 + 1)/2) * 2 / 1 * 0.29'
+ as='int((1 + 2)/2) * 2 / 1 * 0.29' pd='2*int((1 + 1)/2) * (2 / 1 + 0.29)' ps='2*int((1 + 2)/2) * (2 / 1 + 0.29)'
+ nrd='0.29 / 2 ' nrs='0.29 / 2 ' sa=0 sb=0 sd=0 mult=1 m=1
XM81 net48 nb VGND VGND sky130_fd_pr__nfet_01v8 L=1 W=2 nf=1 ad='int((1 + 1)/2) * 2 / 1 * 0.29' as='int((1 + 2)/2) * 2 / 1 * 0.29'
+ pd='2*int((1 + 1)/2) * (2 / 1 + 0.29)' ps='2*int((1 + 2)/2) * (2 / 1 + 0.29)' nrd='0.29 / 2 ' nrs='0.29 / 2 '
+ sa=0 sb=0 sd=0 mult=1 m=1
XM23 net49 net51 net25 VDPWR sky130_fd_pr__pfet_01v8 L=1 W=4 nf=2 ad='int((2 + 1)/2) * 4 / 2 * 0.29'
+ as='int((2 + 2)/2) * 4 / 2 * 0.29' pd='2*int((2 + 1)/2) * (4 / 2 + 0.29)' ps='2*int((2 + 2)/2) * (4 / 2 + 0.29)'
+ nrd='0.29 / 4 ' nrs='0.29 / 4 ' sa=0 sb=0 sd=0 mult=1 m=1
XM56 net36 pcas net49 VDPWR sky130_fd_pr__pfet_01v8 L=0.5 W=2 nf=1 ad='int((1 + 1)/2) * 2 / 1 * 0.29'
+ as='int((1 + 2)/2) * 2 / 1 * 0.29' pd='2*int((1 + 1)/2) * (2 / 1 + 0.29)' ps='2*int((1 + 2)/2) * (2 / 1 + 0.29)'
+ nrd='0.29 / 2 ' nrs='0.29 / 2 ' sa=0 sb=0 sd=0 mult=1 m=1
XM82 net50 net51 net25 VDPWR sky130_fd_pr__pfet_01v8 L=1 W=4 nf=2 ad='int((2 + 1)/2) * 4 / 2 * 0.29'
+ as='int((2 + 2)/2) * 4 / 2 * 0.29' pd='2*int((2 + 1)/2) * (4 / 2 + 0.29)' ps='2*int((2 + 2)/2) * (4 / 2 + 0.29)'
+ nrd='0.29 / 4 ' nrs='0.29 / 4 ' sa=0 sb=0 sd=0 mult=1 m=1
XM83 net51 pcas net50 VDPWR sky130_fd_pr__pfet_01v8 L=0.5 W=2 nf=1 ad='int((1 + 1)/2) * 2 / 1 * 0.29'
+ as='int((1 + 2)/2) * 2 / 1 * 0.29' pd='2*int((1 + 1)/2) * (2 / 1 + 0.29)' ps='2*int((1 + 2)/2) * (2 / 1 + 0.29)'
+ nrd='0.29 / 2 ' nrs='0.29 / 2 ' sa=0 sb=0 sd=0 mult=1 m=1
XC4 net36 pinm sky130_fd_pr__cap_mim_m3_1 W=6 L=6 MF=1 m=1
XM5 net40 midm net55 VDPWR sky130_fd_pr__pfet_01v8_lvt L=0.5 W=1.5 nf=1 ad='int((1 + 1)/2) * 1.5 / 1 * 0.29'
+ as='int((1 + 2)/2) * 1.5 / 1 * 0.29' pd='2*int((1 + 1)/2) * (1.5 / 1 + 0.29)' ps='2*int((1 + 2)/2) * (1.5 / 1 + 0.29)'
+ nrd='0.29 / 1.5 ' nrs='0.29 / 1.5 ' sa=0 sb=0 sd=0 mult=2 m=2
XM62 net40 ncas net52 VGND sky130_fd_pr__nfet_01v8 L=0.5 W=2 nf=1 ad='int((1 + 1)/2) * 2 / 1 * 0.29'
+ as='int((1 + 2)/2) * 2 / 1 * 0.29' pd='2*int((1 + 1)/2) * (2 / 1 + 0.29)' ps='2*int((1 + 2)/2) * (2 / 1 + 0.29)'
+ nrd='0.29 / 2 ' nrs='0.29 / 2 ' sa=0 sb=0 sd=0 mult=2 m=2
XM84 net52 net54 VGND VGND sky130_fd_pr__nfet_01v8 L=1 W=2 nf=1 ad='int((1 + 1)/2) * 2 / 1 * 0.29' as='int((1 + 2)/2) * 2 / 1 * 0.29'
+ pd='2*int((1 + 1)/2) * (2 / 1 + 0.29)' ps='2*int((1 + 2)/2) * (2 / 1 + 0.29)' nrd='0.29 / 2 ' nrs='0.29 / 2 '
+ sa=0 sb=0 sd=0 mult=2 m=2
XM87 net54 ncas net53 VGND sky130_fd_pr__nfet_01v8 L=0.5 W=2 nf=1 ad='int((1 + 1)/2) * 2 / 1 * 0.29'
+ as='int((1 + 2)/2) * 2 / 1 * 0.29' pd='2*int((1 + 1)/2) * (2 / 1 + 0.29)' ps='2*int((1 + 2)/2) * (2 / 1 + 0.29)'
+ nrd='0.29 / 2 ' nrs='0.29 / 2 ' sa=0 sb=0 sd=0 mult=2 m=2
XM88 net53 net54 VGND VGND sky130_fd_pr__nfet_01v8 L=1 W=2 nf=1 ad='int((1 + 1)/2) * 2 / 1 * 0.29' as='int((1 + 2)/2) * 2 / 1 * 0.29'
+ pd='2*int((1 + 1)/2) * (2 / 1 + 0.29)' ps='2*int((1 + 2)/2) * (2 / 1 + 0.29)' nrd='0.29 / 2 ' nrs='0.29 / 2 '
+ sa=0 sb=0 sd=0 mult=2 m=2
XM89 net56 pb net37 VDPWR sky130_fd_pr__pfet_01v8 L=1 W=4 nf=2 ad='int((2 + 1)/2) * 4 / 2 * 0.29' as='int((2 + 2)/2) * 4 / 2 * 0.29'
+ pd='2*int((2 + 1)/2) * (4 / 2 + 0.29)' ps='2*int((2 + 2)/2) * (4 / 2 + 0.29)' nrd='0.29 / 4 ' nrs='0.29 / 4 '
+ sa=0 sb=0 sd=0 mult=2 m=2
XM90 net55 pcas net56 VDPWR sky130_fd_pr__pfet_01v8 L=0.5 W=2 nf=1 ad='int((1 + 1)/2) * 2 / 1 * 0.29'
+ as='int((1 + 2)/2) * 2 / 1 * 0.29' pd='2*int((1 + 1)/2) * (2 / 1 + 0.29)' ps='2*int((1 + 2)/2) * (2 / 1 + 0.29)'
+ nrd='0.29 / 2 ' nrs='0.29 / 2 ' sa=0 sb=0 sd=0 mult=2 m=2
XM91 net40 ncas net57 VGND sky130_fd_pr__nfet_01v8 L=0.5 W=2 nf=1 ad='int((1 + 1)/2) * 2 / 1 * 0.29'
+ as='int((1 + 2)/2) * 2 / 1 * 0.29' pd='2*int((1 + 1)/2) * (2 / 1 + 0.29)' ps='2*int((1 + 2)/2) * (2 / 1 + 0.29)'
+ nrd='0.29 / 2 ' nrs='0.29 / 2 ' sa=0 sb=0 sd=0 mult=2 m=2
XM92 net57 nb VGND VGND sky130_fd_pr__nfet_01v8 L=1 W=2 nf=1 ad='int((1 + 1)/2) * 2 / 1 * 0.29' as='int((1 + 2)/2) * 2 / 1 * 0.29'
+ pd='2*int((1 + 1)/2) * (2 / 1 + 0.29)' ps='2*int((1 + 2)/2) * (2 / 1 + 0.29)' nrd='0.29 / 2 ' nrs='0.29 / 2 '
+ sa=0 sb=0 sd=0 mult=2 m=2
XC1 net58 midp sky130_fd_pr__cap_mim_m3_1 W=22 L=15 MF=1 m=1
XC2 net59 net41 sky130_fd_pr__cap_mim_m3_1 W=12 L=12 MF=1 m=1
XC3 net60 net40 sky130_fd_pr__cap_mim_m3_1 W=12 L=12 MF=1 m=1
XR1 out net58 VGND sky130_fd_pr__res_xhigh_po_1p41 L=1.5 mult=1 m=1
XR2 net58 net59 VGND sky130_fd_pr__res_xhigh_po_1p41 L=2 mult=1 m=1
XR3 net58 net60 VGND sky130_fd_pr__res_xhigh_po_1p41 L=2 mult=1 m=1
Vmidn midp net62 0
.save i(vmidn)
Vmidp net61 midp 0
.save i(vmidp)
XM94 net41 EN net37 VDPWR sky130_fd_pr__pfet_01v8_hvt L=0.15 W=0.42 nf=1 ad='int((1 + 1)/2) * 0.42 / 1 * 0.29'
+ as='int((1 + 2)/2) * 0.42 / 1 * 0.29' pd='2*int((1 + 1)/2) * (0.42 / 1 + 0.29)' ps='2*int((1 + 2)/2) * (0.42 / 1 + 0.29)'
+ nrd='0.29 / 0.42 ' nrs='0.29 / 0.42 ' sa=0 sb=0 sd=0 mult=1 m=1
XM93 net40 EN net37 VDPWR sky130_fd_pr__pfet_01v8_hvt L=0.15 W=0.42 nf=1 ad='int((1 + 1)/2) * 0.42 / 1 * 0.29'
+ as='int((1 + 2)/2) * 0.42 / 1 * 0.29' pd='2*int((1 + 1)/2) * (0.42 / 1 + 0.29)' ps='2*int((1 + 2)/2) * (0.42 / 1 + 0.29)'
+ nrd='0.29 / 0.42 ' nrs='0.29 / 0.42 ' sa=0 sb=0 sd=0 mult=1 m=1
XM55d net31 VGND VGND VGND sky130_fd_pr__nfet_01v8 L=1 W=2 nf=1 ad='int((1 + 1)/2) * 2 / 1 * 0.29' as='int((1 + 2)/2) * 2 / 1 * 0.29'
+ pd='2*int((1 + 1)/2) * (2 / 1 + 0.29)' ps='2*int((1 + 2)/2) * (2 / 1 + 0.29)' nrd='0.29 / 2 ' nrs='0.29 / 2 '
+ sa=0 sb=0 sd=0 mult=2 m=2
XM13d net6 VGND VGND VGND sky130_fd_pr__nfet_01v8 L=1 W=2 nf=1 ad='int((1 + 1)/2) * 2 / 1 * 0.29' as='int((1 + 2)/2) * 2 / 1 * 0.29'
+ pd='2*int((1 + 1)/2) * (2 / 1 + 0.29)' ps='2*int((1 + 2)/2) * (2 / 1 + 0.29)' nrd='0.29 / 2 ' nrs='0.29 / 2 '
+ sa=0 sb=0 sd=0 mult=2 m=2
XM51d pinm net25 net25 VDPWR sky130_fd_pr__pfet_01v8 L=1 W=4 nf=1 ad='int((1 + 1)/2) * 4 / 1 * 0.29'
+ as='int((1 + 2)/2) * 4 / 1 * 0.29' pd='2*int((1 + 1)/2) * (4 / 1 + 0.29)' ps='2*int((1 + 2)/2) * (4 / 1 + 0.29)'
+ nrd='0.29 / 4 ' nrs='0.29 / 4 ' sa=0 sb=0 sd=0 mult=2 m=2
XM54d pinp net25 net25 VDPWR sky130_fd_pr__pfet_01v8 L=1 W=4 nf=1 ad='int((1 + 1)/2) * 4 / 1 * 0.29'
+ as='int((1 + 2)/2) * 4 / 1 * 0.29' pd='2*int((1 + 1)/2) * (4 / 1 + 0.29)' ps='2*int((1 + 2)/2) * (4 / 1 + 0.29)'
+ nrd='0.29 / 4 ' nrs='0.29 / 4 ' sa=0 sb=0 sd=0 mult=2 m=2
XM40d ninp VGND VGND VGND sky130_fd_pr__nfet_01v8 L=1 W=2 nf=1 ad='int((1 + 1)/2) * 2 / 1 * 0.29' as='int((1 + 2)/2) * 2 / 1 * 0.29'
+ pd='2*int((1 + 1)/2) * (2 / 1 + 0.29)' ps='2*int((1 + 2)/2) * (2 / 1 + 0.29)' nrd='0.29 / 2 ' nrs='0.29 / 2 '
+ sa=0 sb=0 sd=0 mult=2 m=2
**.ends

* expanding   symbol:  /foss/designs/ttsky26c-analog-park/xschem/bias.sym # of pins=5
** sym_path: xschem/bias.sym
** sch_path: xschem/bias.sch
.subckt bias VDPWR pIout VGND EN vbias
*.ipin EN
*.opin pIout
*.ipin VGND
*.ipin VDPWR
*.opin vbias
XM4 inm vbias VDPWR VDPWR sky130_fd_pr__pfet_01v8_lvt L=2 W=2 nf=1 ad='int((1 + 1)/2) * 2 / 1 * 0.29'
+ as='int((1 + 2)/2) * 2 / 1 * 0.29' pd='2*int((1 + 1)/2) * (2 / 1 + 0.29)' ps='2*int((1 + 2)/2) * (2 / 1 + 0.29)'
+ nrd='0.29 / 2 ' nrs='0.29 / 2 ' sa=0 sb=0 sd=0 mult=2 m=2
XM2 inp vbias VDPWR VDPWR sky130_fd_pr__pfet_01v8_lvt L=2 W=2 nf=1 ad='int((1 + 1)/2) * 2 / 1 * 0.29'
+ as='int((1 + 2)/2) * 2 / 1 * 0.29' pd='2*int((1 + 1)/2) * (2 / 1 + 0.29)' ps='2*int((1 + 2)/2) * (2 / 1 + 0.29)'
+ nrd='0.29 / 2 ' nrs='0.29 / 2 ' sa=0 sb=0 sd=0 mult=2 m=2
XM5 pIout vbias VDPWR VDPWR sky130_fd_pr__pfet_01v8_lvt L=2 W=2 nf=1 ad='int((1 + 1)/2) * 2 / 1 * 0.29'
+ as='int((1 + 2)/2) * 2 / 1 * 0.29' pd='2*int((1 + 1)/2) * (2 / 1 + 0.29)' ps='2*int((1 + 2)/2) * (2 / 1 + 0.29)'
+ nrd='0.29 / 2 ' nrs='0.29 / 2 ' sa=0 sb=0 sd=0 mult=2 m=2
XM8 inm inm VGND VGND sky130_fd_pr__nfet_01v8 L=2 W=4 nf=1 ad='int((1 + 1)/2) * 4 / 1 * 0.29' as='int((1 + 2)/2) * 4 / 1 * 0.29'
+ pd='2*int((1 + 1)/2) * (4 / 1 + 0.29)' ps='2*int((1 + 2)/2) * (4 / 1 + 0.29)' nrd='0.29 / 4 ' nrs='0.29 / 4 '
+ sa=0 sb=0 sd=0 mult=1 m=1
XM9 inp inp net1 VGND sky130_fd_pr__nfet_01v8 L=2 W=4 nf=1 ad='int((1 + 1)/2) * 4 / 1 * 0.29' as='int((1 + 2)/2) * 4 / 1 * 0.29'
+ pd='2*int((1 + 1)/2) * (4 / 1 + 0.29)' ps='2*int((1 + 2)/2) * (4 / 1 + 0.29)' nrd='0.29 / 4 ' nrs='0.29 / 4 '
+ sa=0 sb=0 sd=0 mult=4 m=4
XM10 net2 inp VGND VGND sky130_fd_pr__nfet_01v8 L=2 W=2 nf=1 ad='int((1 + 1)/2) * 2 / 1 * 0.29' as='int((1 + 2)/2) * 2 / 1 * 0.29'
+ pd='2*int((1 + 1)/2) * (2 / 1 + 0.29)' ps='2*int((1 + 2)/2) * (2 / 1 + 0.29)' nrd='0.29 / 2 ' nrs='0.29 / 2 '
+ sa=0 sb=0 sd=0 mult=2 m=2
XM11 vbias inm VGND VGND sky130_fd_pr__nfet_01v8 L=2 W=2 nf=1 ad='int((1 + 1)/2) * 2 / 1 * 0.29' as='int((1 + 2)/2) * 2 / 1 * 0.29'
+ pd='2*int((1 + 1)/2) * (2 / 1 + 0.29)' ps='2*int((1 + 2)/2) * (2 / 1 + 0.29)' nrd='0.29 / 2 ' nrs='0.29 / 2 '
+ sa=0 sb=0 sd=0 mult=2 m=2
XM15 vbias startup inm VGND sky130_fd_pr__nfet_01v8_lvt L=0.15 W=0.5 nf=1 ad='int((1 + 1)/2) * 0.5 / 1 * 0.29'
+ as='int((1 + 2)/2) * 0.5 / 1 * 0.29' pd='2*int((1 + 1)/2) * (0.5 / 1 + 0.29)' ps='2*int((1 + 2)/2) * (0.5 / 1 + 0.29)'
+ nrd='0.29 / 0.5 ' nrs='0.29 / 0.5 ' sa=0 sb=0 sd=0 mult=1 m=1
XM3 startup inm VGND VGND sky130_fd_pr__nfet_01v8 L=0.5 W=0.5 nf=1 ad='int((1 + 1)/2) * 0.5 / 1 * 0.29'
+ as='int((1 + 2)/2) * 0.5 / 1 * 0.29' pd='2*int((1 + 1)/2) * (0.5 / 1 + 0.29)' ps='2*int((1 + 2)/2) * (0.5 / 1 + 0.29)'
+ nrd='0.29 / 0.5 ' nrs='0.29 / 0.5 ' sa=0 sb=0 sd=0 mult=1 m=1
XR1 net4 net1 VGND sky130_fd_pr__res_high_po_0p69 L=6.1 mult=1 m=1
XR2 net5 net4 VGND sky130_fd_pr__res_high_po_0p69 L=6.1 mult=1 m=1
XR3 net6 net5 VGND sky130_fd_pr__res_high_po_0p69 L=6.1 mult=1 m=1
XR4 VGND net6 VGND sky130_fd_pr__res_high_po_0p69 L=6.1 mult=1 m=1
XM1 vbias net2 VDPWR VDPWR sky130_fd_pr__pfet_01v8_lvt L=2 W=2 nf=1 ad='int((1 + 1)/2) * 2 / 1 * 0.29'
+ as='int((1 + 2)/2) * 2 / 1 * 0.29' pd='2*int((1 + 1)/2) * (2 / 1 + 0.29)' ps='2*int((1 + 2)/2) * (2 / 1 + 0.29)'
+ nrd='0.29 / 2 ' nrs='0.29 / 2 ' sa=0 sb=0 sd=0 mult=2 m=2
XM12 net2 net2 VDPWR VDPWR sky130_fd_pr__pfet_01v8_lvt L=2 W=2 nf=1 ad='int((1 + 1)/2) * 2 / 1 * 0.29'
+ as='int((1 + 2)/2) * 2 / 1 * 0.29' pd='2*int((1 + 1)/2) * (2 / 1 + 0.29)' ps='2*int((1 + 2)/2) * (2 / 1 + 0.29)'
+ nrd='0.29 / 2 ' nrs='0.29 / 2 ' sa=0 sb=0 sd=0 mult=2 m=2
XM13 startup startup net3 VDPWR sky130_fd_pr__pfet_01v8_lvt L=3 W=0.42 nf=1 ad='int((1 + 1)/2) * 0.42 / 1 * 0.29'
+ as='int((1 + 2)/2) * 0.42 / 1 * 0.29' pd='2*int((1 + 1)/2) * (0.42 / 1 + 0.29)' ps='2*int((1 + 2)/2) * (0.42 / 1 + 0.29)'
+ nrd='0.29 / 0.42 ' nrs='0.29 / 0.42 ' sa=0 sb=0 sd=0 mult=1 m=1
XM16 startup nEN VGND VGND sky130_fd_pr__nfet_01v8 L=0.15 W=0.5 nf=1 ad='int((1 + 1)/2) * 0.5 / 1 * 0.29'
+ as='int((1 + 2)/2) * 0.5 / 1 * 0.29' pd='2*int((1 + 1)/2) * (0.5 / 1 + 0.29)' ps='2*int((1 + 2)/2) * (0.5 / 1 + 0.29)'
+ nrd='0.29 / 0.5 ' nrs='0.29 / 0.5 ' sa=0 sb=0 sd=0 mult=1 m=1
XM17 vbias EN VDPWR VDPWR sky130_fd_pr__pfet_01v8_hvt L=0.15 W=0.42 nf=1 ad='int((1 + 1)/2) * 0.42 / 1 * 0.29'
+ as='int((1 + 2)/2) * 0.42 / 1 * 0.29' pd='2*int((1 + 1)/2) * (0.42 / 1 + 0.29)' ps='2*int((1 + 2)/2) * (0.42 / 1 + 0.29)'
+ nrd='0.29 / 0.42 ' nrs='0.29 / 0.42 ' sa=0 sb=0 sd=0 mult=1 m=1
XM7 net3 nEN VDPWR VDPWR sky130_fd_pr__pfet_01v8_hvt L=0.15 W=0.42 nf=1 ad='int((1 + 1)/2) * 0.42 / 1 * 0.29'
+ as='int((1 + 2)/2) * 0.42 / 1 * 0.29' pd='2*int((1 + 1)/2) * (0.42 / 1 + 0.29)' ps='2*int((1 + 2)/2) * (0.42 / 1 + 0.29)'
+ nrd='0.29 / 0.42 ' nrs='0.29 / 0.42 ' sa=0 sb=0 sd=0 mult=1 m=1
XM14 VDPWR vbias VDPWR VDPWR sky130_fd_pr__pfet_01v8_lvt L=3 W=4 nf=1 ad='int((1 + 1)/2) * 4 / 1 * 0.29'
+ as='int((1 + 2)/2) * 4 / 1 * 0.29' pd='2*int((1 + 1)/2) * (4 / 1 + 0.29)' ps='2*int((1 + 2)/2) * (4 / 1 + 0.29)'
+ nrd='0.29 / 4 ' nrs='0.29 / 4 ' sa=0 sb=0 sd=0 mult=6 m=6
x1 EN VGND VGND VDPWR VDPWR nEN sky130_fd_sc_hd__inv_1
.ends

.end
